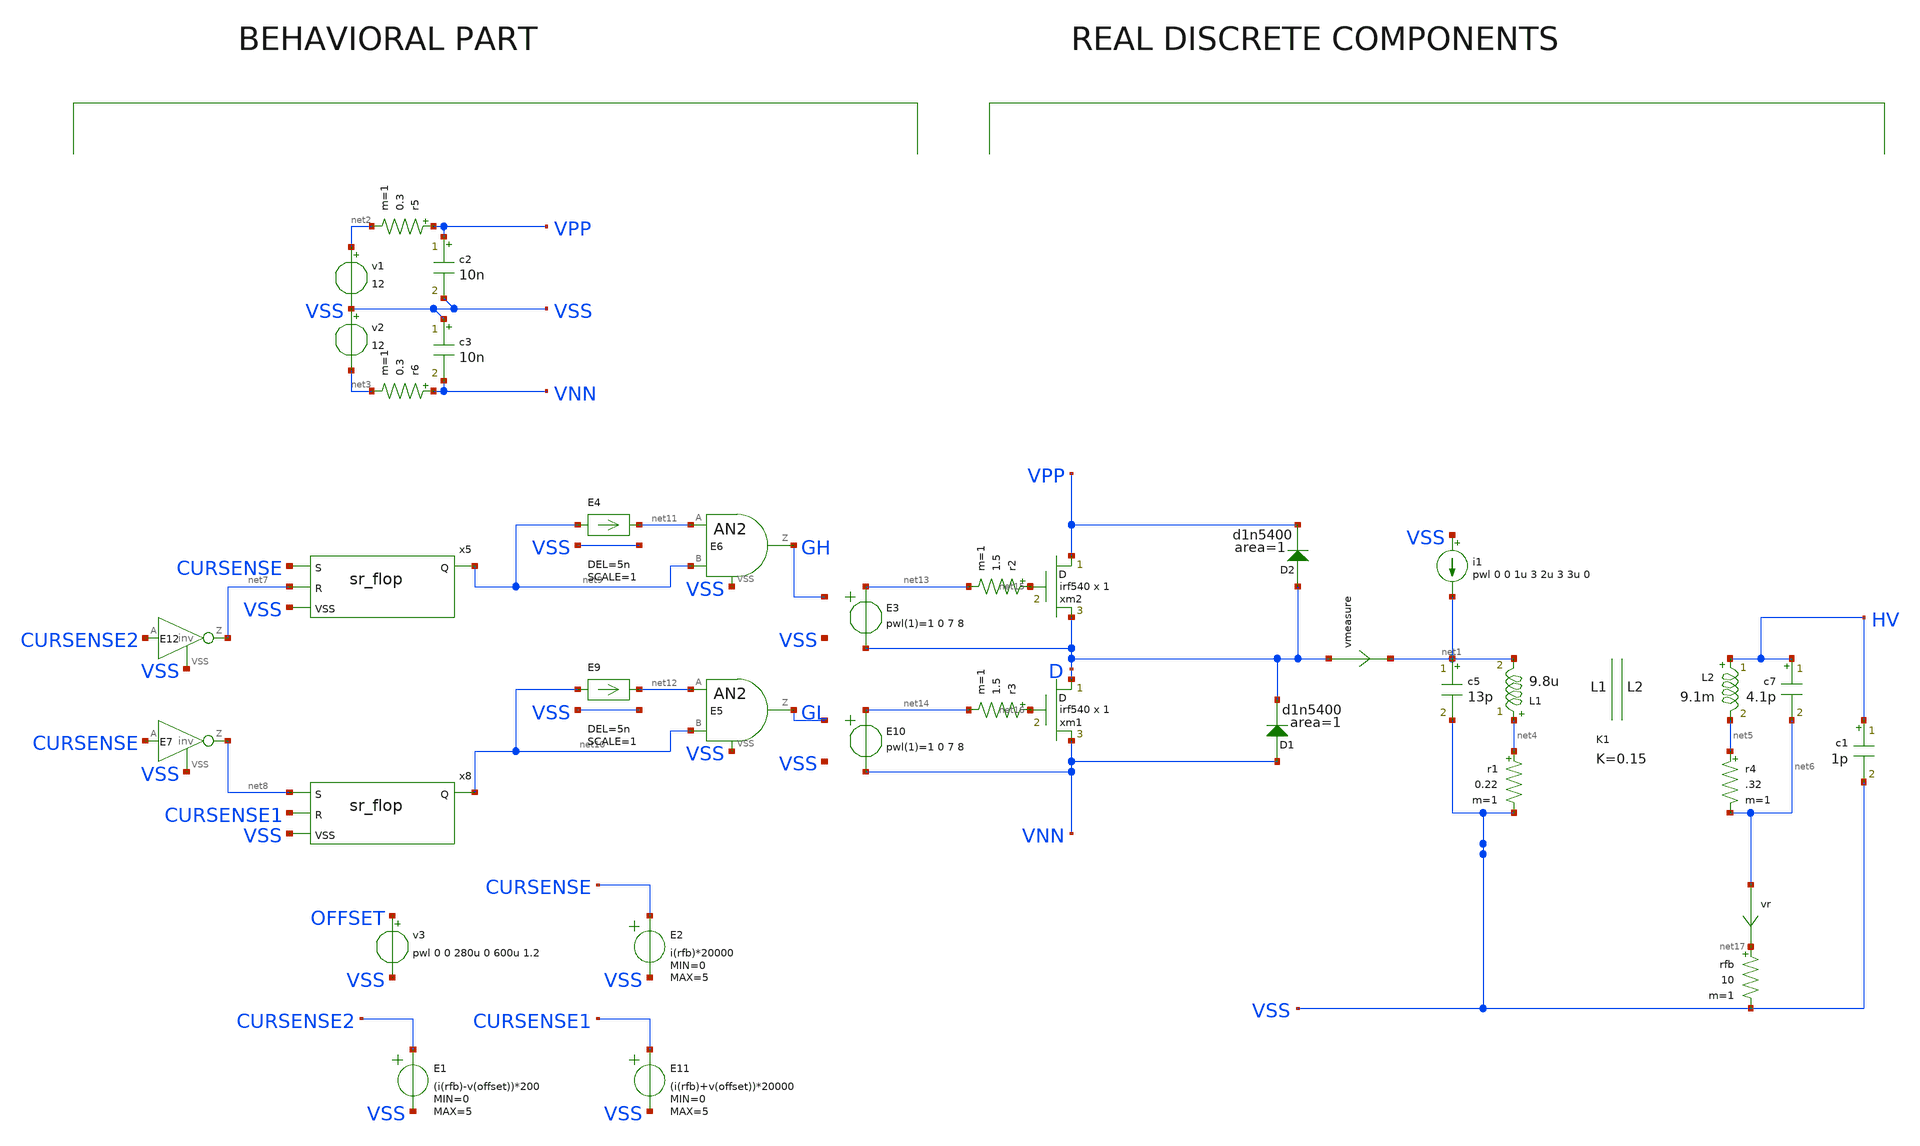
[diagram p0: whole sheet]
** sch_path: xschem_library/examples/tesla2.sch
**.subckt tesla2
vmeasure D net1 0
.probe i( vmeasure )
v1 net2 VSS 12
v2 VSS net3 12
E1 CURSENSE2 VSS VOL=' (i(rfb)-v(offset))*200 ' MIN=' 0 ' MAX=' 5 '
L1 net4 net1 9.8u m=1
r1 net4 VSS 0.22 m=1
c5 net1 VSS 13p m=1
L2 HV net5 9.1m m=1
K1 L1 L2 0.15
r4 net5 net6 .32 m=1
c7 HV net6 4.1p m=1
E11 CURSENSE1 VSS VOL=' (i(rfb)+v(offset))*20000 ' MIN=' 0 ' MAX=' 5 '
v3 OFFSET VSS pwl 0 0 280u 0 600u 1.2
E2 CURSENSE VSS VOL=' i(rfb)*20000 ' MIN=' 0 ' MAX=' 5 '
x8 net8 net10 CURSENSE1 VSS sr_flop VTH=2.5 VHI=5
E7 net8 VSS pwl(1) CURSENSE VSS 2.3 5 2.7 0.0
x5 CURSENSE net9 net7 VSS sr_flop VTH=2.5 VHI=5
E12 net7 VSS pwl(1) CURSENSE2 VSS 2.3 5 2.7 0.0
D1 VNN D d1n5400 area=1
D2 D VPP d1n5400 area=1
c1 HV VSS 1p m=1
c2 VPP VSS 10n m=1
c3 VSS VNN 10n m=1
r5 VPP net2 0.3 m=1
r6 VNN net3 0.3 m=1
E6 GH VSS and(2) net11 VSS net9 VSS 2 0 6 8
E4 net11 VSS DELAY net9 VSS TD=' 5n ' SCALE=' 1 '
E5 GL VSS and(2) net12 VSS net10 VSS 2 0 6 8
E9 net12 VSS DELAY net10 VSS TD=' 5n ' SCALE=' 1 '
xm2 VPP net15 D irf540 m=1
xm1 D net16 VNN irf540 m=1
r2 net15 net13 1.5 m=1
r3 net16 net14 1.5 m=1
E10 net14 VNN pwl(1) GL VSS 1 0 7 8
E3 net13 D pwl(1) GH VSS 1 0 7 8
rfb net17 VSS 10 m=1
i1 VSS net1 pwl 0 0 1u 3 2u 3 3u 0
vr net6 net17 0
.probe i( vr )
**** begin user architecture code

.option PARHIER=LOCAL RUNLVL=6 post MODMONTE=1
.option sampling_method = SRS
.option method=gear
vvss vss 0 dc 0
.temp 30
.tran 20n 1m uic $$ sweep CTUNE 1.5n 8.5n 0.1n

* .meas tran pavg_gatedrv AVG p(xgatedrv) from=950u to=990u
* .meas tran pavg_mos1 AVG p(xmos1) from=950u to=990u
* .meas tran pavg_mos2 AVG p(xmos2) from=950u to=990u
* .probe tran p(xgatedrv) p(xmos1) p(xmos2) i(d1) I(L1) I(L2)
.include stimuli.cir
.probe tran i(l1) i(l2) p(xm1) p(xm2) p(d1) p(d2)

.meas tran pavg_mos1 AVG p(xm1) from=950u to=990u
.meas tran pavg_mos2 AVG p(xm2) from=950u to=990u
.meas tran pavg_d1 AVG p(d1) from=950u to=990u
.meas tran pavg_d2 AVG p(d2) from=950u to=990u


.MODEL bd139_2 npn IS=1e-09 BF=222.664 NF=0.85 VAF=36.4079 IKF=0.166126 ISE=5.03418e-09 NE=1.45313
+ BR=1.35467 NR=1.33751 VAR=142.931 IKR=1.66126 ISC=5.02557e-09 NC=3.10227 RB=26.9143 IRB=0.1 RBM=0.1
+ RE=0.000472454 RC=1.04109 XTB=0.727762 XTI=1.04311 EG=1.05 CJE=1e-11 VJE=0.75 MJE=0.33 TF=1e-09 XTF=1 VTF=10
+ ITF=0.01 CJC=1e-11 VJC=0.75 MJC=0.33 XCJC=0.9 FC=0.5 CJS=0 VJS=0.75 MJS=0.5 TR=1e-07 PTF=0 KF=0 AF=1


.MODEL BD139 NPN ( IS=2.3985E-13 Vceo=80 Icrating=1500m BF=244.9 NF=1.0 BR=78.11 NR=1.007
+ ISE=1.0471E-14 NE=1.2 ISC=1.9314E-11 NC=1.45 VAF=98.5 VAR=7.46 IKF=1.1863 IKR=0.1445 RB=2.14 RBM=0.001 IRB=0.031
+ RE=0.0832 RC=0.01 CJE=2.92702E-10 VJE=0.67412 MJE=0.3300 FC=0.5 CJC=4.8831E-11 VJC=0.5258 MJC=0.3928
+ XCJC=0.5287 XTB=1.1398 EG=1.2105 XTI=3.0)


.MODEL BD140  PNP(IS=1e-09 BF=650.842 NF=0.85 VAF=10 IKF=0.0950125 ISE=1e-08 NE=1.54571 BR=56.177
+ NR=1.5 VAR=2.11267 IKR=0.950125 ISC=1e-08 NC=3.58527 RB=41.7566 IRB=0.1 RBM=0.108893 RE=0.000347052
+ RC=1.32566 XTB=19.5239 XTI=1 EG=1.05 CJE=1e-11 VJE=0.75 MJE=0.33 TF=1e-09 XTF=1 VTF=10 ITF=0.01 CJC=1e-11
+ VJC=0.75 MJC=0.33 XCJC=0.9 FC=0.5 CJS=0 VJS=0.75 MJS=0.5 TR=1e-07 PTF=0 KF=0 AF=10  VCEO=80 ICRATING=1A )


.MODEL Q2N2222A NPN IS =3.0611E-14 NF =1.00124 BF =220 IKF=0.52                VAF=104 ISE=7.5E-15
+ NE =1.41 NR =1.005 BR =4 IKR=0.24                VAR=28 ISC=1.06525E-11 NC =1.3728 RB =0.13 RE =0.22
+                RC =0.12 CJC=9.12E-12 MJC=0.3508 VJC=0.4089                CJE=27.01E-12 TF =0.325E-9 TR =100E-9
+               vce_max=45 vbe_max=6

.MODEL Q2N2222 NPN (  IS = 3.97589E-14 BF = 195.3412 NF = 1.0040078 VAF = 53.081 IKF = 0.976 ISE =
+ 1.60241E-14  NE = 1.4791931 BR = 1.1107942 NR = 0.9928261 VAR = 11.3571702 IKR = 2.4993953 ISC = 1.88505E-12
+  NC = 1.1838278 RB = 56.5826472 IRB = 1.50459E-4 RBM = 5.2592283 RE = 0.0402974 RC = 0.4208  CJE =
+ 2.56E-11 VJE = 0.682256 MJE = 0.3358856 TF = 3.3E-10 XTF = 6 VTF = 0.574  ITF = 0.32 PTF = 25.832 CJC =
+ 1.40625E-11 VJC = 0.5417393 MJC = 0.4547893 XCJC = 1  TR = 3.2E-7 CJS = 0 VJS = .75 MJS = 0 XTB = 1.6486 EG =
+ 1.11  XTI = 5.8315 KF = 0 AF = 1 FC = 0.83               vce_max=45 vbe_max=6 )


* 2n2222 p complementary
.MODEL Q2N2907P PNP(IS=650.6E-18 ISE=54.81E-15 ISC=0 XTI=3  BF=231.7 BR=3.563 IKF=1.079 IKR=0
+ XTB=1.5  VAF=115.7 VAR=35 VJE=0.65 VJC=0.65  RE=0.15 RC=0.715 RB=10  CJE=19.82E-12 CJC=14.76E-12 XCJC=0.75
+ FC=0.5  NF=1 NR=1 NE=1.829 NC=2 MJE=0.3357 MJC=0.5383  TF=603.7E-12 TR=111.3E-9 ITF=0.65 VTF=5 XTF=1.7
+  EG=1.11 KF=1E-9 AF=1  VCEO=45 ICRATING=100M                vce_max=45 vbe_max=6 )

.MODEL Q2N2907S PNP(IS=2.32E-13 ISE=6.69E-16 ISC=1.65E-13 XTI=3.00  BF=3.08E2 BR=2.18E1 IKF=8.42E-1
+ IKR=1.00 XTB=1.5  VAF=1.41E2 VAR=1.35E1 VJE=3.49E-1 VJC=3.00E-1  RE=1.00E-2 RC=8.46E-1 RB=4.02E1 RBM=1.00E-2
+ IRB=1.25E-2  CJE=2.66E-11 CJC=1.93E-11 XCJC=1.00 FC=5.00E-1  NF=1.04 NR=1.12 NE=1.09 NC=1.13 MJE=4.60E-1
+ MJC=4.65E-1  TF=4.95E-10 TR=0 PTF=0 ITF=3.36E-1 VTF=6.54 XTF=1.87E1  EG=1.11 KF=1E-9 AF=1  VCEO=40
+ ICRATING=500M                vce_max=45 vbe_max=6 )

*MM3725 MCE 5/13/95
*Si    1W  40V 500mA 307MHz pkg:TO-39 3,2,1
.MODEL QMM3725 NPN (IS=50.7F NF=1 BF=162 VAF=113 IKF=.45 ISE=38.2P NE=2  BR=4 NR=1 VAR=24 IKR=.675
+ RE=.263 RB=1.05 RC=.105 XTB=1.5  CJE=62.2P VJE=1.1 MJE=.5 CJC=14.6P VJC=.3 MJC=.3 TF=518P TR=45.9N)

*MPS651 MCE 5/12/95
*Si 625mW  60V    2A 110MHz pkg:TO-92 1,2,3
.MODEL QMPS651 NPN (IS=72.1F NF=1 BF=260 VAF=139 IKF=2.5 ISE=67.1P NE=2  BR=4 NR=1 VAR=20 IKR=3.75
+ RE=28.2M RB=.113 RC=11.3M XTB=1.5  CJE=212P VJE=1.1 MJE=.5 CJC=68.6P VJC=.3 MJC=.3 TF=1.44N TR=1U)

*FCX649 ZETEX Spice model   Last revision  17/7/90   Medium Power
*ZTX Si  1.5W  25V    2A 240MHz pkg:SOT-89 2,1,3
.MODEL QFCX649 NPN(IS=3E-13 BF=225 VAF=80 IKF=2.8 ISE=1.1E-13 NE=1.37   BR=110 NR=0.972 VAR=28
+ IKR=0.8 ISC=6.5E-13 NC=1.372 RB=0.3 RE=0.063   RC=0.07 CJE=3.25E-10 TF=1E-9 CJC=7E-11 TR=1E-8 )

*MPSW01A MCE 5/12/95
*Si    1W  40V    1A 210MHz pkg:TO-92 1,2,3
.MODEL QMPSW01A NPN (IS=18.1F NF=1 BF=273 VAF=113 IKF=.6 ISE=15.7P NE=2  BR=4 NR=1 VAR=20 IKR=.9
+ RE=96.5M RB=.386 RC=38.6M XTB=1.5  CJE=78.7P VJE=1.1 MJE=.5 CJC=17.3P VJC=.3 MJC=.3 TF=757P TR=526N)

*BC546 ZETEX Spice model     Last revision  4/90   General Purpose
*ZTX Si 500mW  65V 200mA 300MHz pkg:TO-92 1,2,3
.MODEL BC546 NPN(IS=1.8E-14 BF=400 NF=0.9955 VAF=80 IKF=0.14 ISE=5E-14   NE=1.46 BR=35.5 NR=1.005
+ VAR=12.5 IKR=0.03 ISC=1.72E-13 NC=1.27 RB=0.56   RE=0.6 RC=0.25 CJE=1.3E-11 TF=6.4E-10 CJC=4E-12 VJC=0.54
+ TR=5.072E-8       vce_max=65 vbe_max=6 )


.MODEL BC556 PNP(       IS=2.059E-14      NF=1.003      ISE=2.971E-15      NE=1.316      BF=227.3
+      IKF=0.08719      VAF=37.2      NR=1.007      ISC=1.339E-14      NC=1.15      BR=7.69      IKR=0.07646
+      VAR=11.42      RB=1      IRB=1E-06      RBM=1      RE=0.688      RC=0.6437      XTB=0      EG=1.11      XTI=3
+      CJE=1.4E-11      VJE=0.5912      MJE=0.3572      TF=7.046E-10      XTF=4.217      VTF=5.367      ITF=0.1947
+      PTF=0      CJC=1.113E-11      VJC=0.1      MJC=0.3414      XCJC=0.6288      TR=1E-32      CJS=0
+      VJS=0.75      MJS=0.333      FC=0.7947      vce_max=65 vbe_max=6 )
*

* NXP Semiconductors
*
* Medium power NPN transistor
* IC   = 1 A
* VCEO = 20 V
* hFE  = 85 - 375 @ 2V/500mA
*
*
*
*
* Package pinning does not match Spice model pinning.
* Package: SOT 223
*
* Package Pin 1: Base
* Package Pin 2: Collector
* Package Pin 3: Emitter
* Package Pin 4: Collector
*
* Extraction date (week/year): 13/2008
* Simulator: Spice 3
*
**********************************************************
*#
.SUBCKT BCP68 1 2 3
*
Q1 1 2 3 BCP68
D1 2 1 DIODE
*
*The diode does not reflect a
*physical device but improves
*only modeling in the reverse
*mode of operation.
*
.MODEL BCP68 NPN   IS = 2.312E-013   NF = 0.988   ISE = 8.851E-014   NE = 2.191   BF = 273   IKF =
+ 5.5   VAF = 50   NR = 0.9885   ISC = 6.808E-014   NC = 3   BR = 155.6   IKR = 4   VAR = 17   RB = 15
+   IRB = 2E-006   RBM = 0.65   RE = 0.073   RC = 0.073   XTB = 0   EG = 1.11   XTI = 3   CJE = 2.678E-010
+   VJE = 0.732   MJE = 0.3484   TF = 5.8E-010   XTF = 1.5   VTF = 2.5   ITF = 1   PTF = 0   CJC =
+ 3.406E-011   VJC = 2   MJC = 0.3142   XCJC = 1   TR = 6.5E-009   CJS = 0   VJS = 0.75   MJS = 0.333   FC =
+ 0.95
.MODEL DIODE D   IS = 2.702E-015   N = 1.2   BV = 1000   IBV = 0.001   RS = 0.1   CJO = 0   VJ = 1
+   M = 0.5   FC = 0   TT = 0   EG = 1.11   XTI = 3
.ENDS

.model D1N4007 D(IS=7.02767n RS=0.0341512 N=1.80803 EG=1.05743 XTI=5 BV=1000 IBV=5e-08 CJO=1e-11
+ VJ=0.7 M=0.5 FC=0.5 TT=1e-07 )

.MODEL D1N4148 D   IS = 4.352E-9   N = 1.906   BV = 110   IBV = 0.0001   RS = 0.6458   CJO =
+ 7.048E-13   VJ = 0.869   M = 0.03   FC = 0.5   TT = 3.48E-9

.MODEL D1n5400 d IS=2.61339e-12 RS=0.0110501 N=1.20576 EG=0.6 XTI=3.1271 BV=50 IBV=1e-05 CJO=1e-11
+ VJ=0.7 M=0.5 FC=0.5 TT=1e-09 KF=0 AF=1
* Model generated on October 12, 2003
* Model format: PSpice

*1N758
*Ref: Motorola
*10V 500mW Si Zener pkg:DIODE0.4 1,2
.MODEL D1N758 D(IS=1E-11 RS=8.483 N=1.27 TT=5E-8 CJO=2.334E-10 VJ=0.75   M=0.33 BV=9.83 IBV=0.01 )

*1N4744
*Ref: Motorola
*15V 1W Si Zener pkg:DIODE0.4 1,2
.MODEL D1N4744 D(IS=5.32E-14 RS=6.47 TT=5.01E-8 CJO=7.83E-11 M=0.33   BV=14.89 IBV=0.017 )

*1N755
*Ref: Motorola
*7.5V 500mW Si Zener pkg:DIODE0.4 1,2
.MODEL D1N755 D(IS=1E-11 RS=3.359 N=1.27 TT=5E-8 CJO=2.959E-10 VJ=0.75   M=0.33 BV=7.433 IBV=0.01 )

** node order
* 1: gnd
* 2: trig
* 3: out
* 4: reset#
* 5: ctrl
* 6: thres
* 7: dis
* 8: vcc
.SUBCKT ne555  34 32 30 19 23 33 1  21
*              G  TR O  R  F  TH D  V
Q4 25 2 3 QP
Q5 34 6 3 QP
Q6 6 6 8 QP
R1 9 21 4.7K
R2 3 21 830
R3 8 21 4.7K
Q7 2 33 5 QN
Q8 2 5 17 QN
Q9 6 4 17 QN
Q10 6 23 4 QN
Q11 12 20 10 QP
R4 10 21 1K
Q12 22 11 12 QP
Q13 14 13 12 QP
Q14 34 32 11 QP
Q15 14 18 13 QP
R5 14 34 100K
R6 22 34 100K
R7 17 34 10K
Q16 1 15 34 QN
Q17 15 19 31 QP
R8 18 23 5K
R9 18 34 5K
R10 21 23 5K
Q18 27 20 21 QP
Q19 20 20 21 QP
R11 20 31 5K
D1 31 24 DA
Q20 24 25 34 QN
Q21 25 22 34 QN
Q22 27 24 34 QN
R12 25 27 4.7K
R13 21 29 6.8K
Q23 21 29 28 QN
Q24 29 27 16 QN
Q25 30 26 34 QN
Q26 21 28 30 QN
D2 30 29 DA
R14 16 15 100
R15 16 26 220
R16 16 34 4.7K
R17 28 30 3.9K
Q3 2 2 9 QP
.MODEL DA D (RS=40 IS=1.0E-14 CJO=1PF)
.MODEL QP PNP (level=1 BF=20 BR=0.02 RC=4 RB=25 IS=1.0E-14 VA=50 NE=2)  CJE=12.4P VJE=1.1 MJE=.5
+ CJC=4.02P VJC=.3 MJC=.3 TF=229P TR=159N)
.MODEL QN NPN (level=1 IS=5.07F NF=1 BF=100 VAF=161 IKF=30M ISE=3.9P NE=2  BR=4 NR=1 VAR=16 IKR=45M
+ RE=1.03 RB=4.12 RC=.412 XTB=1.5  CJE=12.4P VJE=1.1 MJE=.5 CJC=4.02P VJC=.3 MJC=.3 TF=229P TR=959P)
.ENDS

.SUBCKT BS250P 3 4 5
*              D G S
M1 3 2 5 5 MBS250
RG 4 2 160
RL 3 5 1.2E8
C1 2 5 47E-12
C2 3 2 10E-12
D1 3 5 DBS250
*
.MODEL MBS250 PMOS VTO=-3.193 RS=2.041 RD=0.697 IS=1E-15 KP=0.277 CBD=105E-12 PB=1 LAMBDA=1.2E-2
.MODEL DBS250 D IS=2E-13 RS=0.309
.ENDS BS250P

.SUBCKT BS170 3 4 5
*             D G S
M1 3 2 5 5 N3306M
RG 4 2 270
RL 3 5 1.2E8
C1 2 5 28E-12
C2 3 2 3E-12
D1 5 3 N3306D
*
.MODEL N3306M NMOS VTO=1.824 RS=1.572 RD=1.436 IS=1E-15 KP=.1233 CBD=35E-12 PB=1
.MODEL N3306D D IS=5E-12 RS=.768
.ENDS BS170
*

*$
.SUBCKT PTON_TOFF_U4_S1 1 2 3 4
G_Switch 3 4 VCR PWL(1) 1 2 0.2 100e6 0.8 1m
RS_U4_S1         1 2 1G
.ENDS PTON_TOFF_U4_S1
*$
.SUBCKT PTON_TOFF_U4_S2 1 2 3 4
G_Switch 3 4 VCR PWL(1) 1 2 0.2 100e6 0.8 1m
RS_U4_S2         1 2 1G
.ENDS PTON_TOFF_U4_S2
*$
.SUBCKT MTON_TOFF_U2_S2 1 2 3 4
G_Switch 3 4 VCR PWL(1) 1 2 0.2 100e6 0.8 1m
RS_U2_S2         1 2 1G
.ENDS MTON_TOFF_U2_S2
*$
.SUBCKT MTON_TOFF_U2_S1 1 2 3 4
G_Switch 3 4 VCR PWL(1) 1 2 0.2 100e6 0.8 1m
RS_U2_S1         1 2 1G
.ENDS MTON_TOFF_U2_S1
*$
****************************** Basic Components **************************
.SUBCKT D_D1 1 2
D1 1 2 DD1
.MODEL DD1 D (IS=1e-15 Rs=0.001 N=0.1  TT=10p)
.ENDS D_D1
*$
.SUBCKT BUF_BASIC_GEN A  Y VDD=1 VSS=0 VTHRESH=0.5
* E_ABMGATE    YINT 0 vol='V(A) > VTHRESH? VDD:VSS'
E_ABMGATE    YINT 0 pwl(1) A 0 'VTHRESH-0.01' VSS 'VTHRESH+0.01' VDD
RINT YINT Y 1
CINT Y 0 1n
.ENDS BUF_BASIC_GEN
*$
.MODEL NMOS01 NMOS (VTO = 2 KP = 1.005 LAMBDA  = 0.001)
*$
.MODEL PMOS01 PMOS (VTO = -2 KP = 1.77 LAMBDA  = 0.001)
*$
.MODEL NMOS02 NMOS (VTO = 2 KP = 0.1814 LAMBDA = 0.001)
*$
.MODEL PMOS02 PMOS (VTO = -2 KP = 0.2497 LAMBDA = 0.001)
*$
.SUBCKT COMPHYS_BASIC_GEN INP INM HYS OUT VDD=1 VSS=0 VTHRESH=0.5
EIN INP1 INM1 INP INM 1
* EHYS INP1 INP2 vol='V(1) > VTHRESH? -V(HYS):0'
EHYS INP1 INP2 pwl(1) 1 0 'VTHRESH-0.01' 0 'VTHRESH+0.01' '-V(HYS)'

EOUT OUT 0 vol='V(INP2)>V(INM1)? VDD : VSS'
R1 OUT 1 1
C1 1 0 5n
RINP1 INP1 0 1K
.ENDS COMPHYS_BASIC_GEN
*$
.SUBCKT AND2_BASIC_GEN A B Y  VDD=1 VSS=0 VTHRESH=0.5
E_ABMGATE    YINT 0 vol= 'V(A) > VTHRESH  && V(B) > VTHRESH ? VDD:VSS'
RINT YINT Y 1
CINT Y 0 1n
.ENDS AND2_BASIC_GEN
*$
.SUBCKT NOR2_BASIC_GEN A B Y  VDD=1 VSS=0 VTHRESH=0.5
E_ABMGATE    YINT 0 vol= 'V(A) > VTHRESH  || V(B) > VTHRESH ? VSS:VDD'
RINT YINT Y 1
CINT Y 0 1n
.ENDS NOR2_BASIC_GEN
*$
.SUBCKT AND3_BASIC_GEN A B C Y VDD=1 VSS=0 VTHRESH=0.5
E_ABMGATE    YINT 0 vol= 'V(A) > VTHRESH  &&  V(B) > VTHRESH && V(C) > VTHRESH ? VDD:VSS'
RINT YINT Y 1
CINT Y 0 1n
.ENDS AND3_BASIC_GEN
*$
.SUBCKT INV_BASIC_GEN A  Y VDD=1 VSS=0 VTHRESH=0.5
* E_ABMGATE    YINT 0 vol='V(A) > VTHRESH ? VSS : VDD'
E_ABMGATE    YINT 0 pwl(1) A 0 'VTHRESH-0.01' VDD 'VTHRESH+0.01' VSS
RINT YINT Y 1
CINT Y 0 1n
.ENDS INV_BASIC_GEN
*$
.SUBCKT RVAR 101 102 201 202 RREF=1
* nodes : 101 102 : nodes between which variable resistance is placed
* 201 202 : nodes to whose voltage the resistance is proportional
* parameters : rref : reference value of the resistance
rin 201 202 1G   $$ input resistance
r 301 0 rref
fcopy 0 301 vsense 1 $$  copy output current thru Z
eout 101 106 poly(2) 201 202 301 0 0 0 0 0 1   $$ multiply VoverZ with Vctrl
vsense 106 102 0   $$ sense iout
.ENDS RVAR
*$


*LM317 TI voltage regulator - pin order: In, Adj, Out
*TI adjustable voltage regulator pkg:TO-3
.SUBCKT LM317 1 2 3 **Changes my be required on this line**
J1 1 3 4 JN
Q2 5 5 6 QPL .1
Q3 5 8 9 QNL .2
Q4 8 5 7 QPL .1
Q5 81 8 3 QNL .2
Q6 3 81 10 QPL .2
Q7 12 81 13 QNL .2
Q8 10 5 11 QPL .2
Q9 14 12 10 QPL .2
Q10 16 5 17 QPL .2
Q11 16 14 15 QNL .2
Q12 3 20 16 QPL .2
Q13 1 19 20 QNL .2
Q14 19 5 18 QPL .2
Q15 3 21 19 QPL .2
Q16 21 22 16 QPL .2
Q17 21 3 24 QNL .2
Q18 22 22 16 QPL .2
Q19 22 3 241 QNL 2
Q20 3 25 16 QPL .2
Q21 25 26 3 QNL .2
Q22A 35 35 1 QPL 2
Q22B 16 35 1 QPL 2
Q23 35 16 30 QNL 2
Q24A 27 40 29 QNL .2
Q24B 27 40 28 QNL .2
Q25 1 31 41 QNL 5
Q26 1 41 32 QNL 50
D1 3 4 DZ
D2 33 1 DZ
D3 29 34 DZ
R1 1 6 310
R2 1 7 310
R3 1 11 190
R4 1 17 82
R5 1 18 5.6K
R6 4 8 100K
R7 8 81 130
R8 10 12 12.4K
R9 9 3 180
R10 13 3 4.1K
R11 14 3 5.8K
R12 15 3 72
R13 20 3 5.1K
R14 2 24 12K
R15 24 241 2.4K
R16 16 25 6.7K
R17 16 40 12K
R18 30 41 130
R19 16 31 370
R20 26 27 13K
R21 27 40 400
R22 3 41 160
R23 33 34 18K
R24 28 29 160
R25 28 32 3
R26 32 3 .1
C1 21 3 30PF
C2 21 2 30PF
C3 25 26 5PF
CBS1 5 3 2PF
CBS2 35 3 1PF
CBS3 22 3 1PF
.MODEL JN NJF(BETA=1E-4 VTO=-7)
.MODEL DZ D(BV=6.3)
.MODEL QNL NPN(EG=1.22 BF=80 RB=100 CCS=1.5PF TF=.3NS TR=6NS CJE=2PF  CJC=1PF VAF=100)
.MODEL QPL PNP(BF=40 RB=20 TF=.6NS TR=10NS CJE=1.5PF CJC=1PF VAF=50)
.ENDS

.SUBCKT xxxxLM317 1 3 2
* IN ADJ OUT
IADJ 1 4 50U
VREF 4 3 1.25
RC 1 14 0.742
DBK 14 13 D1
CBC 13 15 2.479N
RBC 15 5 247
QP 13 5 2 Q1
RB2 6 5 124
DSC 6 11 D1
ESC 11 2 POLY(2) (13,5) (6,5) 2.85  0 0 0 -70.1M
DFB 6 12 D1
EFB 12 2 POLY(2) (13,5) (6,5) 3.92  -135M 0 1.21M -70.1M
RB1 7 6 1
EB 7 2 8 2 2.56
CPZ 10 2 0.796U
DPU 10 2 D1
RZ 8 10 0.104
RP 9 8 100
EP 9 2 4 2 103.6
RI 2 4 100MEG
.MODEL Q1 NPN (IS=30F BF=100  VAF=14.27 NF=1.604)
.MODEL D1 D (IS=30F N=1.604)
.ENDS



.SUBCKT LM337 8 1 19
*Connections Input Adj. Output
*LM337 negative voltage regulator
.MODEL QN NPN (BF=50 TF=1N CJC=1P)
.MODEL QPOUT PNP (BF=50 TF=1N RE=.2 CJC=1P)
.MODEL QP PNP CJC=1P TF=2N
.MODEL DN D
.MODEL D2 D BV=12 IBV=100U
R10 25 6 1K
Q3 8 17 16 QPOUT
Q4 8 25 17 QP
R18 19 17 250
R19 19 16 .3
G1 8 6 1 18 .1
C7 6 2 .04U
R24 2 8 100
I_ADJ 0 1 65U
R26 8 25 200K
Q5 25 4 19 QP
R27 16 4 200
R28 7 4 7K
D1 8 7 D2
D2 8 6 DN
V1 18 19 1.25
.ENDS


**** end user architecture code
**.ends
.end
